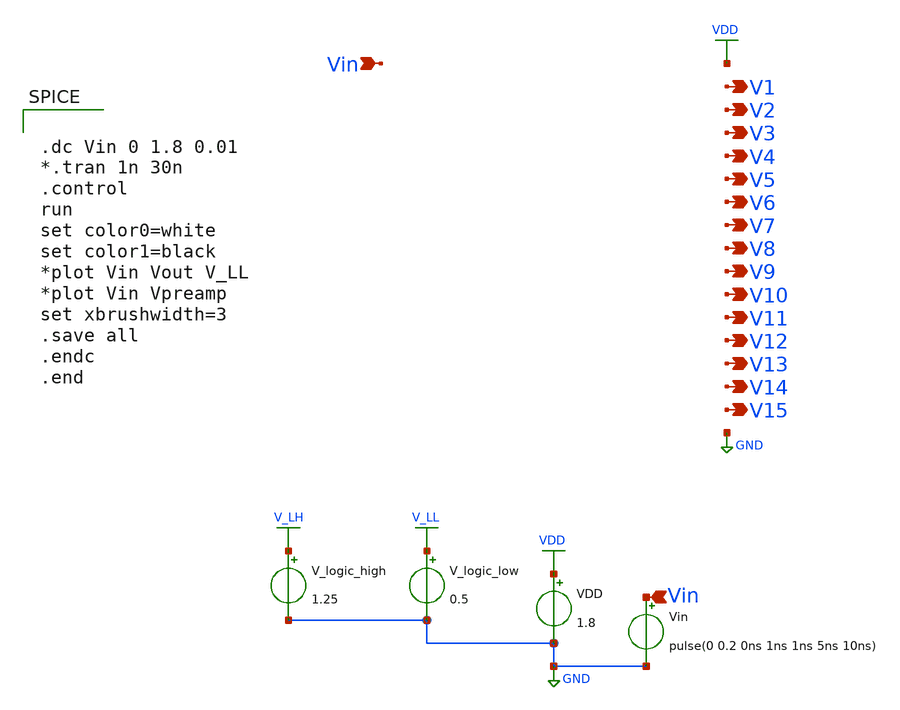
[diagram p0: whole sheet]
** sch_path: xschem/Vth_sch/Pre_layout/Analog_bench.sch
**.subckt Analog_bench Vin Vin V10 V12 V14 V15 V1 V2 V3 V4 V5 V6 V7 V8 V9 V11 V13
*.ipin Vin
*.ipin Vin
*.opin V10
*.opin V12
*.opin V14
*.opin V15
*.opin V1
*.opin V2
*.opin V3
*.opin V4
*.opin V5
*.opin V6
*.opin V7
*.opin V8
*.opin V9
*.opin V11
*.opin V13
VDD VDD GND 1.8
Vin Vin GND pulse(0 0.2 0ns 1ns 1ns 5ns 10ns)
V_logic_high V_LH GND 1.25
V_logic_low V_LL GND 0.5
**** begin user architecture code


.lib /usr/local/share/pdk/sky130A/libs.tech/ngspice/sky130.lib.spice tt
.include /usr/local/share/pdk/sky130A/libs.ref/sky130_fd_sc_hd/spice/sky130_fd_sc_hd.spice
.save all





.dc Vin 0 1.8 0.01
*.tran 1n 30n
.control
run
set color0=white
set color1=black
*plot Vin Vout V_LL
*plot Vin Vpreamp
set xbrushwidth=3
.save all
.endc
.end


**** end user architecture code
**.ends
.GLOBAL VDD
.GLOBAL GND
.GLOBAL V_LH
.GLOBAL V_LL
.end
